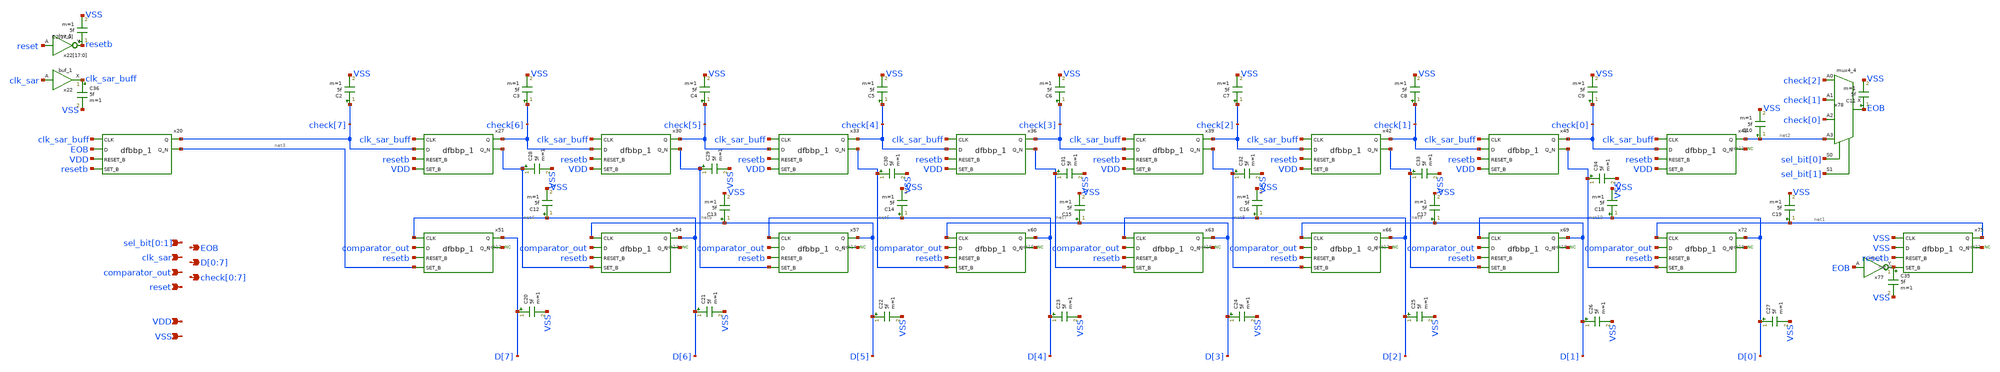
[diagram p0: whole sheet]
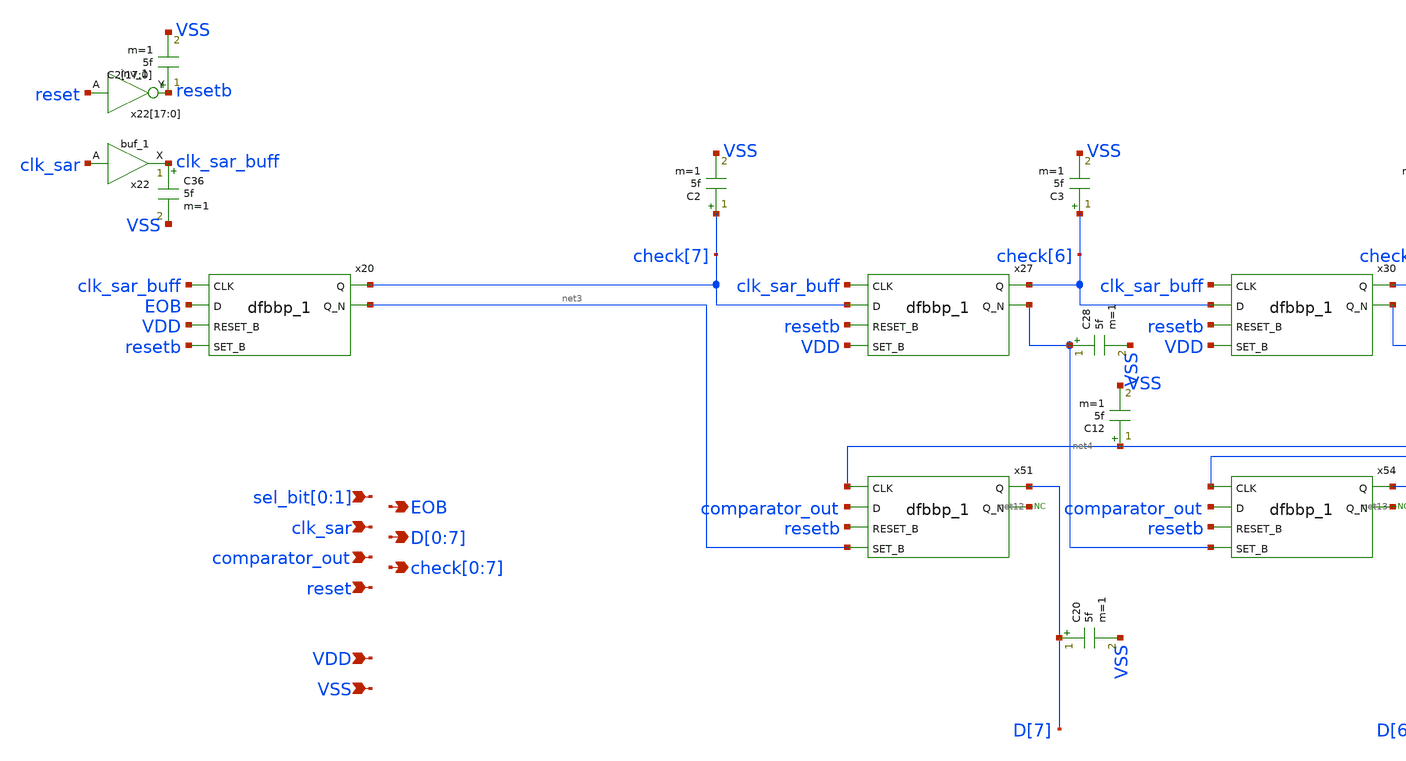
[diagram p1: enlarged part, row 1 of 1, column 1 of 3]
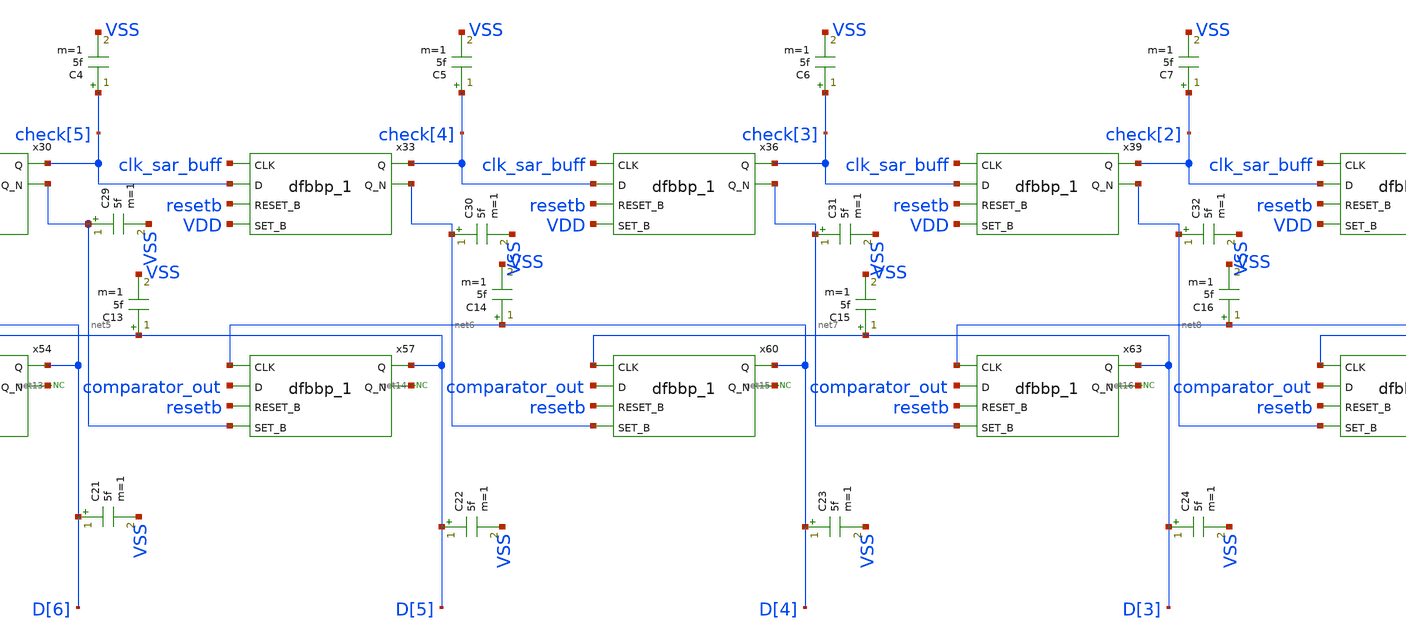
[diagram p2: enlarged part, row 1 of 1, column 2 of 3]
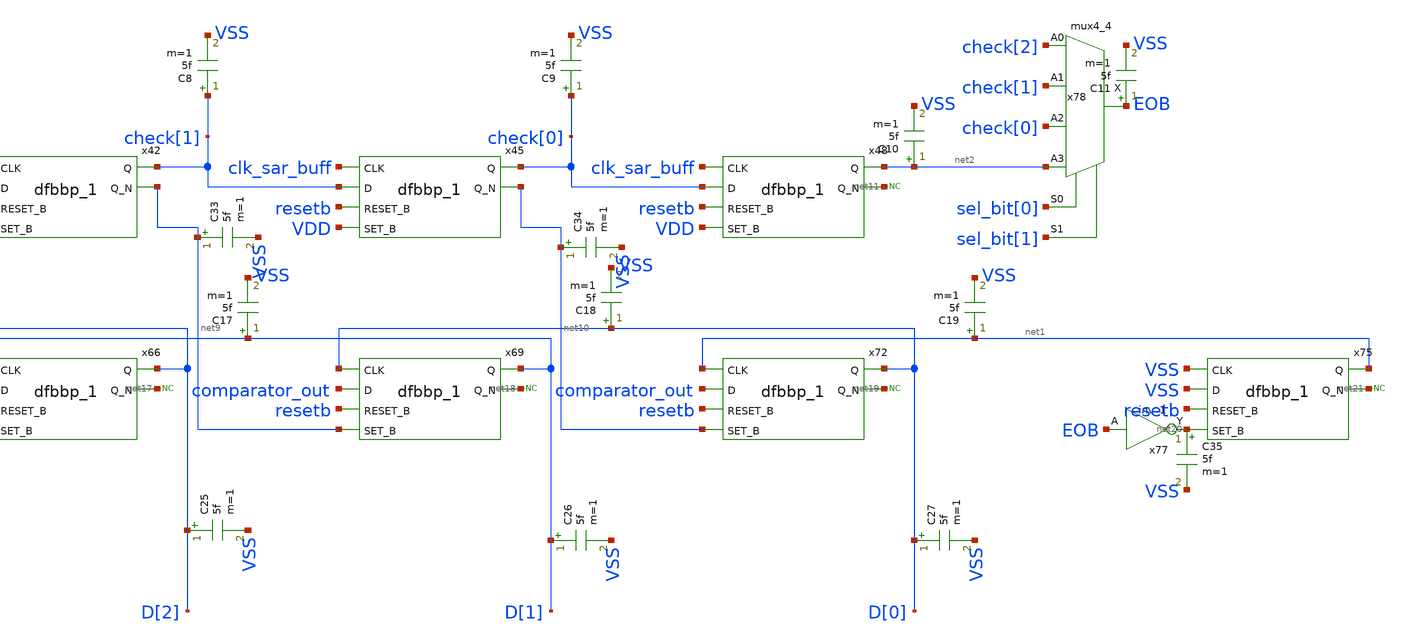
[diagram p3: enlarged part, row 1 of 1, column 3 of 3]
** sch_path: hgu/xschem/8bit_sar_logic.sch
**.subckt 8bit_sar_logic clk_sar VDD VSS comparator_out reset EOB
*+ D[0],D[1],D[2],D[3],D[4],D[5],D[6],D[7] check[0],check[1],check[2],check[3],check[4],check[5],check[6],check[7] sel_bit[0],sel_bit[1]
*.ipin clk_sar
*.ipin VDD
*.ipin VSS
*.ipin comparator_out
*.ipin reset
*.opin EOB
*.opin D[0],D[1],D[2],D[3],D[4],D[5],D[6],D[7]
*.opin check[0],check[1],check[2],check[3],check[4],check[5],check[6],check[7]
*.ipin sel_bit[0],sel_bit[1]
x20 clk_sar_buff EOB VDD resetb VGND VNB VPB VPWR check[7] net3 sky130_fd_sc_hd__dfbbp_1
x27 clk_sar_buff check[7] resetb VDD VGND VNB VPB VPWR check[6] net4 sky130_fd_sc_hd__dfbbp_1
x30 clk_sar_buff check[6] resetb VDD VGND VNB VPB VPWR check[5] net5 sky130_fd_sc_hd__dfbbp_1
x33 clk_sar_buff check[5] resetb VDD VGND VNB VPB VPWR check[4] net6 sky130_fd_sc_hd__dfbbp_1
x36 clk_sar_buff check[4] resetb VDD VGND VNB VPB VPWR check[3] net7 sky130_fd_sc_hd__dfbbp_1
x39 clk_sar_buff check[3] resetb VDD VGND VNB VPB VPWR check[2] net8 sky130_fd_sc_hd__dfbbp_1
x42 clk_sar_buff check[2] resetb VDD VGND VNB VPB VPWR check[1] net9 sky130_fd_sc_hd__dfbbp_1
x45 clk_sar_buff check[1] resetb VDD VGND VNB VPB VPWR check[0] net10 sky130_fd_sc_hd__dfbbp_1
x48 clk_sar_buff check[0] resetb VDD VGND VNB VPB VPWR net2 net11 sky130_fd_sc_hd__dfbbp_1
x51 D[6] comparator_out resetb net3 VGND VNB VPB VPWR D[7] net12 sky130_fd_sc_hd__dfbbp_1
* noconn #net12
x54 D[5] comparator_out resetb net4 VGND VNB VPB VPWR D[6] net13 sky130_fd_sc_hd__dfbbp_1
* noconn #net13
x57 D[4] comparator_out resetb net5 VGND VNB VPB VPWR D[5] net14 sky130_fd_sc_hd__dfbbp_1
* noconn #net14
x60 D[3] comparator_out resetb net6 VGND VNB VPB VPWR D[4] net15 sky130_fd_sc_hd__dfbbp_1
* noconn #net15
x63 D[2] comparator_out resetb net7 VGND VNB VPB VPWR D[3] net16 sky130_fd_sc_hd__dfbbp_1
* noconn #net16
x66 D[1] comparator_out resetb net8 VGND VNB VPB VPWR D[2] net17 sky130_fd_sc_hd__dfbbp_1
* noconn #net17
x69 D[0] comparator_out resetb net9 VGND VNB VPB VPWR D[1] net18 sky130_fd_sc_hd__dfbbp_1
* noconn #net18
x72 net1 comparator_out resetb net10 VGND VNB VPB VPWR D[0] net19 sky130_fd_sc_hd__dfbbp_1
* noconn #net19
x75 VSS VSS resetb net20 VGND VNB VPB VPWR net1 net21 sky130_fd_sc_hd__dfbbp_1
x77 EOB VGND VNB VPB VPWR net20 sky130_fd_sc_hd__inv_1
* noconn #net21
x78 check[2] check[1] check[0] net2 sel_bit[0] sel_bit[1] VGND VNB VPB VPWR EOB
+ sky130_fd_sc_hd__mux4_4
* noconn #net11
x22[17] reset VGND VNB VPB VPWR resetb sky130_fd_sc_hd__inv_1
x22[16] reset VGND VNB VPB VPWR resetb sky130_fd_sc_hd__inv_1
x22[15] reset VGND VNB VPB VPWR resetb sky130_fd_sc_hd__inv_1
x22[14] reset VGND VNB VPB VPWR resetb sky130_fd_sc_hd__inv_1
x22[13] reset VGND VNB VPB VPWR resetb sky130_fd_sc_hd__inv_1
x22[12] reset VGND VNB VPB VPWR resetb sky130_fd_sc_hd__inv_1
x22[11] reset VGND VNB VPB VPWR resetb sky130_fd_sc_hd__inv_1
x22[10] reset VGND VNB VPB VPWR resetb sky130_fd_sc_hd__inv_1
x22[9] reset VGND VNB VPB VPWR resetb sky130_fd_sc_hd__inv_1
x22[8] reset VGND VNB VPB VPWR resetb sky130_fd_sc_hd__inv_1
x22[7] reset VGND VNB VPB VPWR resetb sky130_fd_sc_hd__inv_1
x22[6] reset VGND VNB VPB VPWR resetb sky130_fd_sc_hd__inv_1
x22[5] reset VGND VNB VPB VPWR resetb sky130_fd_sc_hd__inv_1
x22[4] reset VGND VNB VPB VPWR resetb sky130_fd_sc_hd__inv_1
x22[3] reset VGND VNB VPB VPWR resetb sky130_fd_sc_hd__inv_1
x22[2] reset VGND VNB VPB VPWR resetb sky130_fd_sc_hd__inv_1
x22[1] reset VGND VNB VPB VPWR resetb sky130_fd_sc_hd__inv_1
x22[0] reset VGND VNB VPB VPWR resetb sky130_fd_sc_hd__inv_1
x22 clk_sar VGND VNB VPB VPWR clk_sar_buff sky130_fd_sc_hd__buf_1
C2[17] resetb VSS 5f m=1
C2[16] resetb VSS 5f m=1
C2[15] resetb VSS 5f m=1
C2[14] resetb VSS 5f m=1
C2[13] resetb VSS 5f m=1
C2[12] resetb VSS 5f m=1
C2[11] resetb VSS 5f m=1
C2[10] resetb VSS 5f m=1
C2[9] resetb VSS 5f m=1
C2[8] resetb VSS 5f m=1
C2[7] resetb VSS 5f m=1
C2[6] resetb VSS 5f m=1
C2[5] resetb VSS 5f m=1
C2[4] resetb VSS 5f m=1
C2[3] resetb VSS 5f m=1
C2[2] resetb VSS 5f m=1
C2[1] resetb VSS 5f m=1
C2[0] resetb VSS 5f m=1
C2 check[7] VSS 5f m=1
C3 check[6] VSS 5f m=1
C4 check[5] VSS 5f m=1
C5 check[4] VSS 5f m=1
C6 check[3] VSS 5f m=1
C7 check[2] VSS 5f m=1
C8 check[1] VSS 5f m=1
C9 check[0] VSS 5f m=1
C10 net2 VSS 5f m=1
C11 EOB VSS 5f m=1
C12 D[6] VSS 5f m=1
C13 D[5] VSS 5f m=1
C14 D[4] VSS 5f m=1
C15 D[3] VSS 5f m=1
C16 D[2] VSS 5f m=1
C17 D[1] VSS 5f m=1
C18 D[0] VSS 5f m=1
C19 net1 VSS 5f m=1
C20 D[7] VSS 5f m=1
C21 D[6] VSS 5f m=1
C22 D[5] VSS 5f m=1
C23 D[4] VSS 5f m=1
C24 D[3] VSS 5f m=1
C25 D[2] VSS 5f m=1
C26 D[1] VSS 5f m=1
C27 D[0] VSS 5f m=1
C28 net4 VSS 5f m=1
C29 net5 VSS 5f m=1
C30 net6 VSS 5f m=1
C31 net7 VSS 5f m=1
C32 net8 VSS 5f m=1
C33 net9 VSS 5f m=1
C34 net10 VSS 5f m=1
C35 net20 VSS 5f m=1
C36 clk_sar_buff VSS 5f m=1
**.ends
.end
